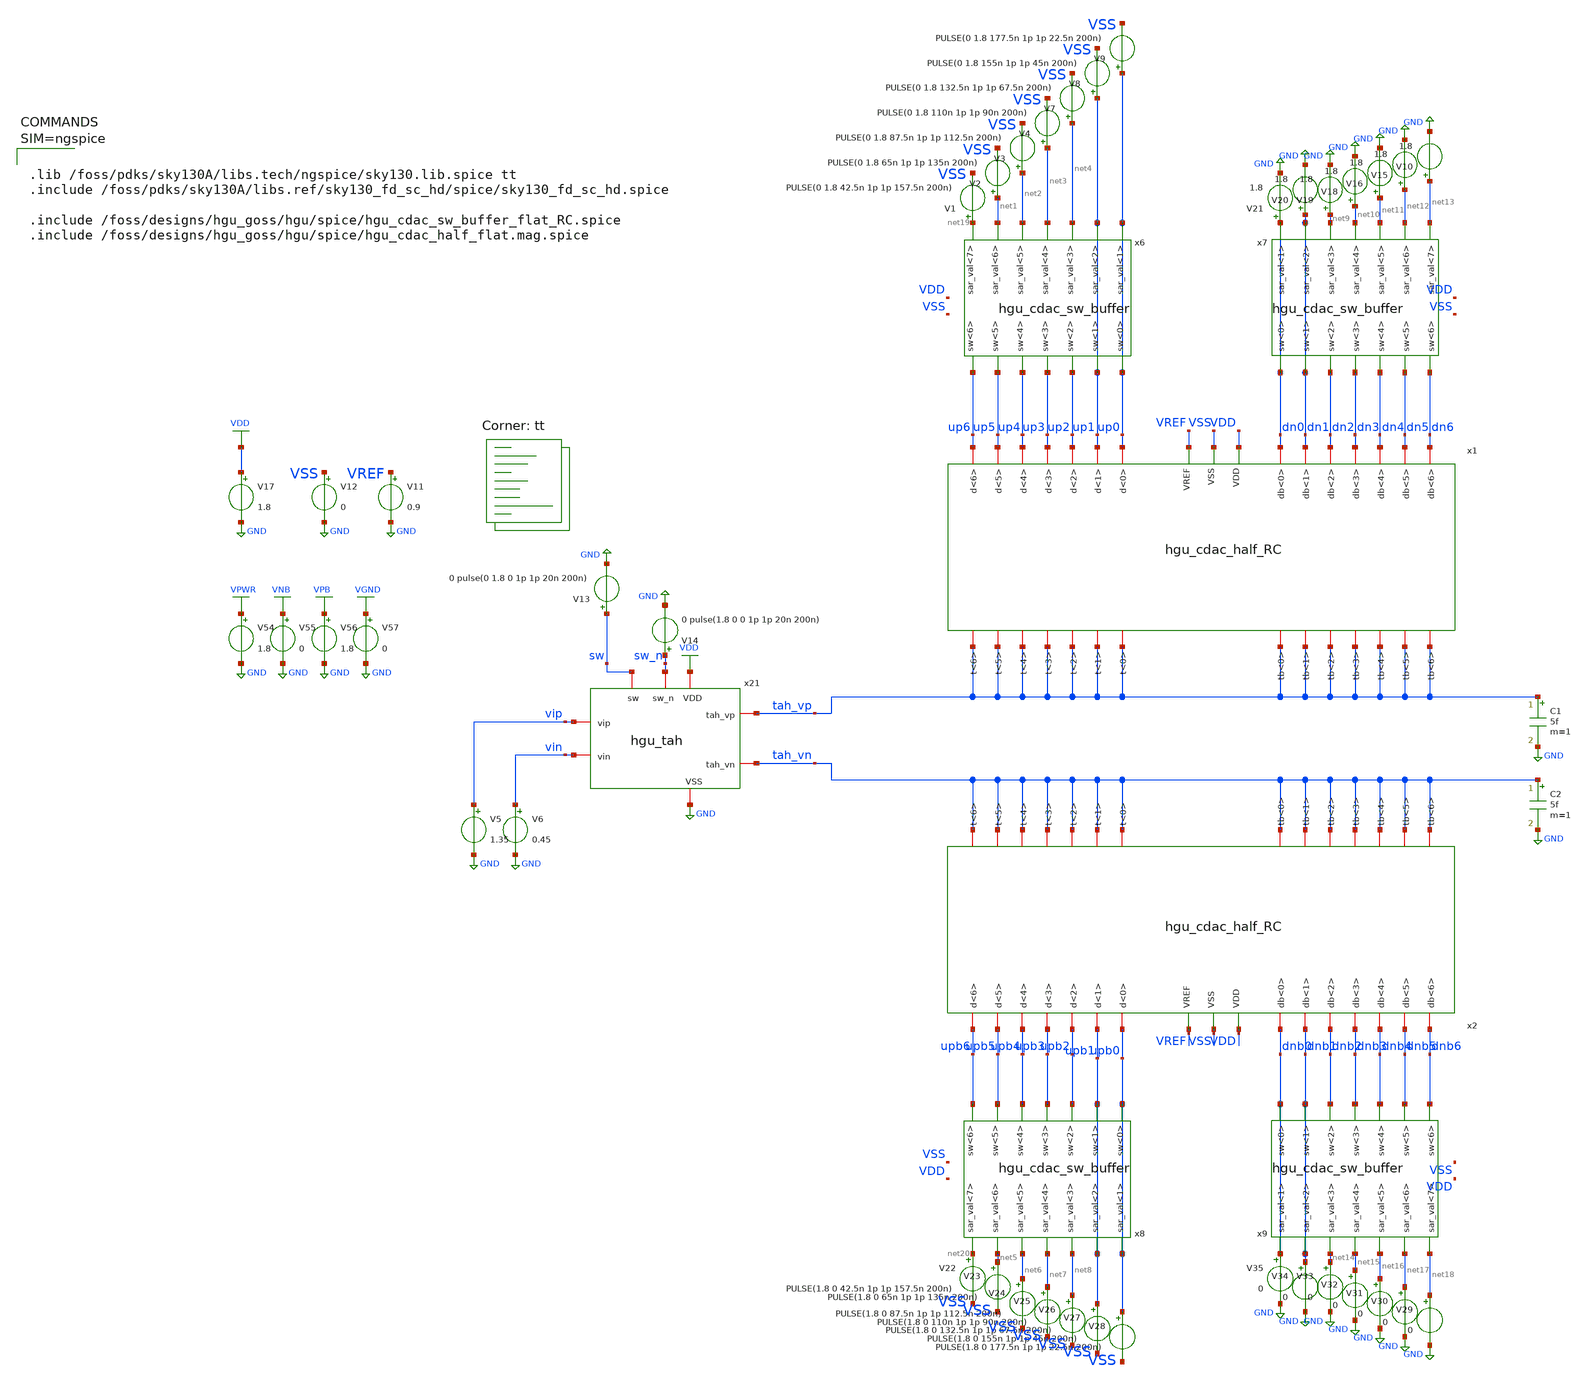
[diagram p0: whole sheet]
** sch_path: hgu/tb/tb_hgu_cdac_8bit.sch
**.subckt tb_hgu_cdac_8bit
x1 up5 dn4 up3 dn1 dn2 up2 dn6 dn5 dn0 up4 up6 up1 up0 dn3 VSS VREF tah_vp tah_vp tah_vp tah_vp
+ tah_vp tah_vp tah_vp tah_vp tah_vp tah_vp tah_vp tah_vp tah_vp tah_vp VDD hgu_cdac_half
x2 upb5 dnb4 upb3 dnb1 dnb2 upb2 dnb6 dnb5 dnb0 upb4 upb6 upb1 upb0 dnb3 VSS VREF tah_vn tah_vn
+ tah_vn tah_vn tah_vn tah_vn tah_vn tah_vn tah_vn tah_vn tah_vn tah_vn tah_vn tah_vn VDD hgu_cdac_half_RC
V1 net19 VSS PULSE(0 1.8 42.5n 1p 1p 157.5n 200n)
V2 net1 VSS PULSE(0 1.8 65n 1p 1p 135n 200n)
C1 tah_vp GND 5f m=1
C2 tah_vn GND 5f m=1
V11 VREF GND 0.9
V12 VSS GND 0
x21 sw VDD GND sw_n tah_vp vip vin tah_vn hgu_tah
V13 sw GND 0 pulse(0 1.8 0 1p 1p 20n 200n)
V14 sw_n GND 0 pulse(1.8 0 0 1p 1p 20n 200n)
V17 VDD GND 1.8
V3 net2 VSS PULSE(0 1.8 87.5n 1p 1p 112.5n 200n)
V4 net3 VSS PULSE(0 1.8 110n 1p 1p 90n 200n)
V7 net4 VSS PULSE(0 1.8 132.5n 1p 1p 67.5n 200n)
V8 up1 VSS PULSE(0 1.8 155n 1p 1p 45n 200n)
V9 up0 VSS PULSE(0 1.8 177.5n 1p 1p 22.5n 200n)
V10 net13 GND 1.8
V15 net12 GND 1.8
V16 net11 GND 1.8
V18 net10 GND 1.8
V19 net9 GND 1.8
V20 dn1 GND 1.8
V21 dn0 GND 1.8
V22 net20 VSS PULSE(1.8 0 42.5n 1p 1p 157.5n 200n)
V23 net5 VSS PULSE(1.8 0 65n 1p 1p 135n 200n)
V24 net6 VSS PULSE(1.8 0 87.5n 1p 1p 112.5n 200n)
V25 net7 VSS PULSE(1.8 0 110n 1p 1p 90n 200n)
V26 net8 VSS PULSE(1.8 0 132.5n 1p 1p 67.5n 200n)
V27 upb1 VSS PULSE(1.8 0 155n 1p 1p 45n 200n)
V28 upb0 VSS PULSE(1.8 0 177.5n 1p 1p 22.5n 200n)
V29 net18 GND 0
V30 net17 GND 0
V31 net16 GND 0
V32 net15 GND 0
V33 net14 GND 0
V34 dnb1 GND 0
V35 dnb0 GND 0
V5 vip GND 1.35
V6 vin GND 0.45
x6 net4 net1 up0 up1 net3 net2 net19 up1 up2 up5 up3 up0 up4 up6 hgu_cdac_sw_buffer
x7 net9 net12 dn0 dn1 net10 net11 net13 dn1 dn2 dn5 dn3 dn0 dn4 dn6 hgu_cdac_sw_buffer
x8 net8 net5 upb0 upb1 net7 net6 net20 upb1 upb2 upb5 upb3 upb0 upb4 upb6 hgu_cdac_sw_buffer
x9 net14 net17 dnb0 dnb1 net15 net16 net18 dnb1 dnb2 dnb5 dnb3 dnb0 dnb4 dnb6 hgu_cdac_sw_buffer
V54 VPWR GND 1.8
V55 VNB GND 0
V56 VPB GND 1.8
V57 VGND GND 0
**** begin user architecture code


.save all
.temp = 25
.tran 60p 200n
.OPTIONS savecurrents

.include /foss/pdks/sky130A/libs.ref/sky130_fd_sc_hd/spice/sky130_fd_sc_hd.spice
.include /foss/designs/hgu_goss/hgu/mag/hgu_cdac_unit.spice
.include /foss/designs/hgu_goss/hgu/spice/hgu_cdac_half_flat.mag.spice


.control
	run
        plot v(up6)+56 v(up5)+54 v(up4)+52 v(up3)+50 v(up2)+48 v(up1)+46 v(up0)+44 v(dn6)+42
+ v(dn5)+40 v(dn4)+38 v(dn3)+36 v(dn2)+34 v(dn1)+32 v(dn0)+30 v(upb6)+28 v(upb5)+26 v(upb4)+24 v(upb3)+22
+ v(upb2)+20 v(upb1)+18 v(upb0)+16 v(dnb6)+14 v(dnb5)+12 v(dnb4)+10 v(dnb3)+8 v(dnb2)+6 v(dnb1)+4 v(dnb0)+2
	plot v(sw) v(tah_vp)-v(tah_vn) vip vin

.endc


.lib $::SKYWATER_MODELS/sky130.lib.spice tt



.lib /foss/pdks/sky130A/libs.tech/ngspice/sky130.lib.spice tt
.include /foss/pdks/sky130A/libs.ref/sky130_fd_sc_hd/spice/sky130_fd_sc_hd.spice

.include /foss/designs/hgu_goss/hgu/spice/hgu_cdac_sw_buffer_flat_RC.spice
.include /foss/designs/hgu_goss/hgu/spice/hgu_cdac_half_flat.mag.spice



**** end user architecture code
**.ends

* expanding   symbol:  ../xschem/hgu_cdac_sw_buffer.sym # of pins=14
** sym_path: hgu/xschem/hgu_cdac_sw_buffer.sym
** sch_path: hgu/xschem/hgu_cdac_sw_buffer.sch
.subckt hgu_cdac_sw_buffer sar_val<3> sar_val<6> sar_val<1> sar_val<2> sar_val<4> sar_val<5>
+ sar_val<7> sw<1> sw<2> sw<5> sw<3> sw<0> sw<4> sw<6>
*.ipin sar_val<7>
*.opin sw<6>
*.opin sw<5>
*.opin sw<4>
*.opin sw<3>
*.opin sw<2>
*.opin sw<1>
*.opin sw<0>
*.ipin sar_val<6>
*.ipin sar_val<5>
*.ipin sar_val<4>
*.ipin sar_val<3>
*.ipin sar_val<2>
*.ipin sar_val<1>
x6 sar_val<3> VGND VNB VPB VPWR sw<2> sky130_fd_sc_hd__buf_1
x7 sar_val<5> VGND VNB VPB VPWR net1 sky130_fd_sc_hd__buf_1
x9 sar_val<7> VGND VNB VPB VPWR net2 sky130_fd_sc_hd__buf_1
x8 net1 VGND VNB VPB VPWR sw<4> sky130_fd_sc_hd__buf_4
x10 net2 VGND VNB VPB VPWR net3 sky130_fd_sc_hd__buf_4
x11 net3 VGND VNB VPB VPWR sw<6> sky130_fd_sc_hd__buf_16
x12 sar_val<4> VGND VNB VPB VPWR sw<3> sky130_fd_sc_hd__buf_1
x13 sar_val<6> VGND VNB VPB VPWR net4 sky130_fd_sc_hd__buf_1
x14 net4 VGND VNB VPB VPWR sw<5> sky130_fd_sc_hd__buf_4
x1 sar_val<1> VGND VNB VPB VPWR sw<0> sky130_fd_sc_hd__buf_1
x2 sar_val<2> VGND VNB VPB VPWR sw<1> sky130_fd_sc_hd__buf_1
.ends

.GLOBAL GND
.GLOBAL VDD
.GLOBAL VGND
.GLOBAL VNB
.GLOBAL VPB
.GLOBAL VPWR
.end
